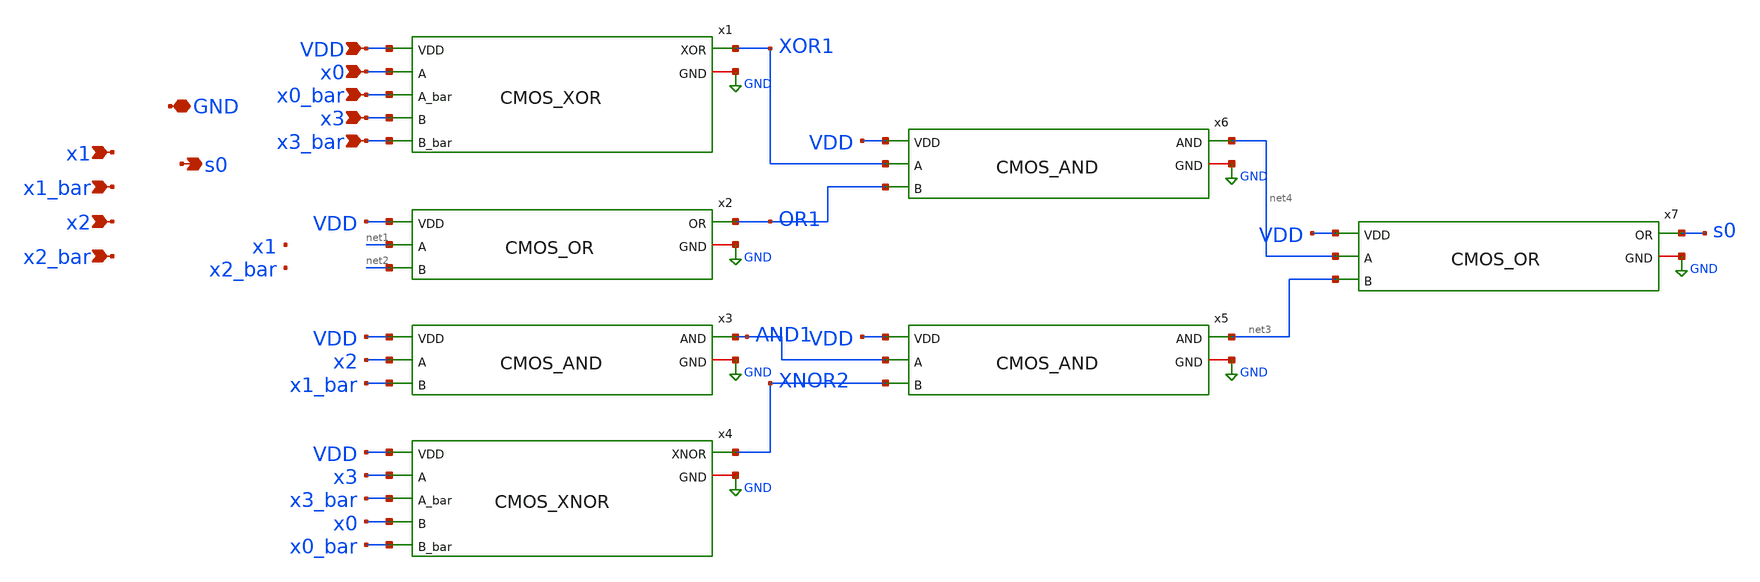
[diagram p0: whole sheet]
** sch_path: skywater_stuff/untitled-10.sch
**.subckt untitled-10 VDD GND s0 x0 x0_bar x1 x1_bar x2 x2_bar x3_bar x3
*.ipin VDD
*.iopin GND
*.opin s0
*.ipin x0
*.ipin x0_bar
*.ipin x1
*.ipin x1_bar
*.ipin x2
*.ipin x2_bar
*.ipin x3_bar
*.ipin x3
x1 x0 x0_bar x3 x3_bar XOR1 GND VDD CMOS_XOR
x2 net1 net2 OR1 GND VDD CMOS_OR
x3 x2 x1_bar AND1 GND VDD CMOS_AND
x4 x3 x3_bar x0 x0_bar XNOR2 GND VDD CMOS_XNOR
x5 AND1 XNOR2 net3 GND VDD CMOS_AND
x6 XOR1 OR1 net4 GND VDD CMOS_AND
x7 net4 net3 s0 GND VDD CMOS_OR
**.ends
.GLOBAL GND
.end
